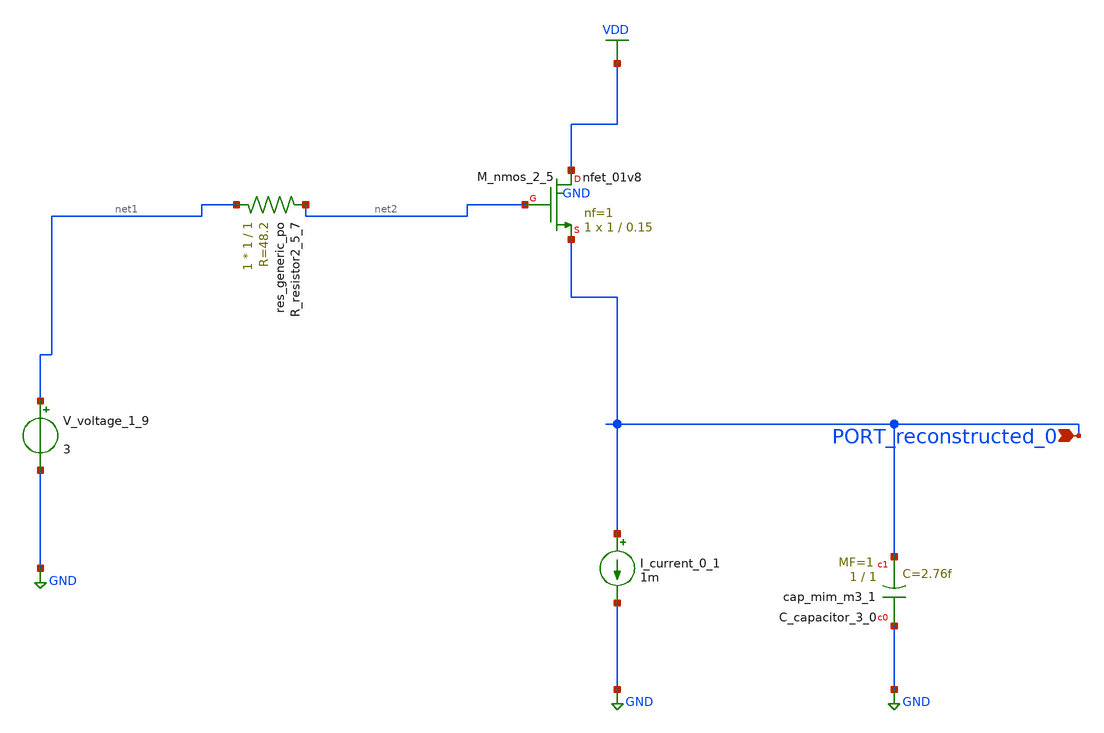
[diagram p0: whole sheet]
** sch_path: schematics/AMSNet/368.sch
**.subckt 368 PORT_reconstructed_0
*.ipin PORT_reconstructed_0
XC_capacitor_3_0 GND PORT_reconstructed_0 sky130_fd_pr__cap_mim_m3_1 W=1 L=1 MF=1 m=1
I_current_0_1 PORT_reconstructed_0 GND 1m
XM_nmos_2_5 VDD net2 PORT_reconstructed_0 GND sky130_fd_pr__nfet_01v8 L=0.15 W=1 nf=1 ad='int((1 + 1)/2) * 1 / 1 * 0.29'
+ as='int((1 + 2)/2) * 1 / 1 * 0.29' pd='2*int((1 + 1)/2) * (1 / 1 + 0.29)' ps='2*int((1 + 2)/2) * (1 / 1 + 0.29)'
+ nrd='0.29 / 1 ' nrs='0.29 / 1 ' sa=0 sb=0 sd=0 mult=1 m=1
XR_resistor2_5_7 net1 net2 sky130_fd_pr__res_generic_po W=1 L=1 m=1
V_voltage_1_9 net1 GND 3
**.ends
.GLOBAL GND
.GLOBAL VDD
.end
